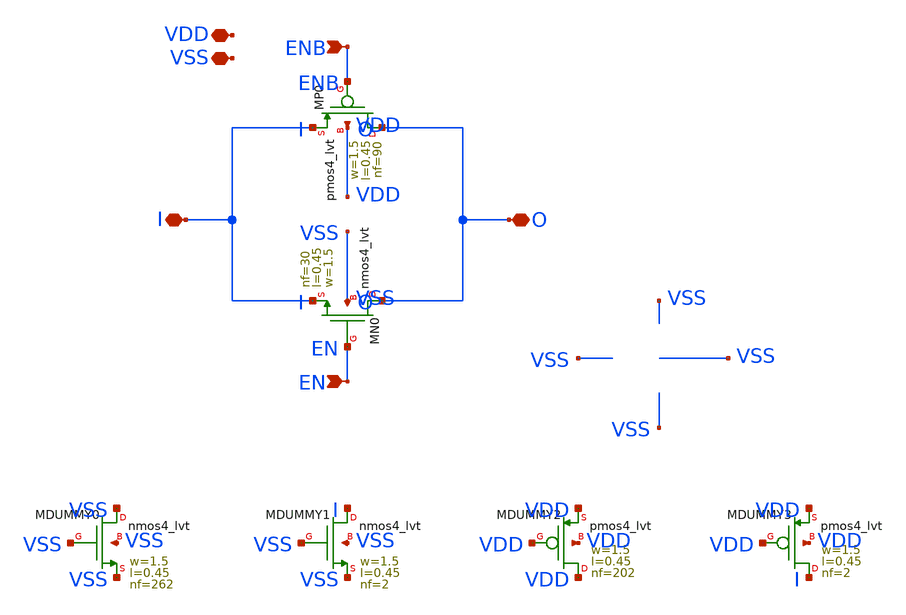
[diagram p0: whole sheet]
** sch_path: xschem/mux_2to1_generated_sky130_fd_pr/tgate/tgate.sch
**.subckt tgate EN ENB I O VDD VSS
*.ipin EN
*.ipin ENB
*.iopin I
*.iopin O
*.iopin VDD
*.iopin VSS
XMN0 O EN I VSS nmos4_lvt w=1.5 l=0.45 nf=30
XMP0 O ENB I VDD pmos4_lvt w=1.5 l=0.45 nf=90
XMDUMMY0 VSS VSS VSS VSS nmos4_lvt w=1.5 l=0.45 nf=262
XMDUMMY1 I VSS VSS VSS nmos4_lvt w=1.5 l=0.45 nf=2
XMDUMMY2 VDD VDD VDD VDD pmos4_lvt w=1.5 l=0.45 nf=202
XMDUMMY3 I VDD VDD VDD pmos4_lvt w=1.5 l=0.45 nf=2
**.ends

* expanding   symbol:  mux_2to1_generated_sky130_fd_pr/BAG_prim/nmos4_lvt/nmos4_lvt.sym # of pins=4
** sym_path: xschem/mux_2to1_generated_sky130_fd_pr/BAG_prim/nmos4_lvt/nmos4_lvt.sym
** sch_path: xschem/mux_2to1_generated_sky130_fd_pr/BAG_prim/nmos4_lvt/nmos4_lvt.sch
.subckt nmos4_lvt D G S B model
w=100n
l=18n
nf=4
model=nmos4_lvt


*.iopin D
*.iopin G
*.iopin S
*.iopin B
MM1 D G S B sky130_fd_pr__nfet_01v8_lvt L=l W='w * nf ' nf=nf ad='int((nf+1)/2) * W * 0.29u' as='int((nf+2)/2) * W * 0.29u'
+ pd='2*int((nf+1)/2) * (W + 0.29u)' ps='2*int((nf+2)/2) * (W + 0.29u)' nrd='0.29u*nf / W' nrs='0.29u*nf / W'
+ sa=0 sb=0 sd=0 mult=1 m=1
.ends


* expanding   symbol:  mux_2to1_generated_sky130_fd_pr/BAG_prim/pmos4_lvt/pmos4_lvt.sym # of pins=4
** sym_path: xschem/mux_2to1_generated_sky130_fd_pr/BAG_prim/pmos4_lvt/pmos4_lvt.sym
** sch_path: xschem/mux_2to1_generated_sky130_fd_pr/BAG_prim/pmos4_lvt/pmos4_lvt.sch
.subckt pmos4_lvt D G S B model
w=100n
l=18n
nf=4
model=pmos4_lvt


*.iopin D
*.iopin G
*.iopin S
*.iopin B
MM1 D G S B sky130_fd_pr__pfet_01v8_lvt L=l W='w * nf ' nf=nf ad='int((nf+1)/2) * W * 0.29u' as='int((nf+2)/2) * W * 0.29u'
+ pd='2*int((nf+1)/2) * (W + 0.29u)' ps='2*int((nf+2)/2) * (W + 0.29u)' nrd='0.29u*nf / W' nrs='0.29u*nf / W'
+ sa=0 sb=0 sd=0 mult=1 m=1
.ends

.end
